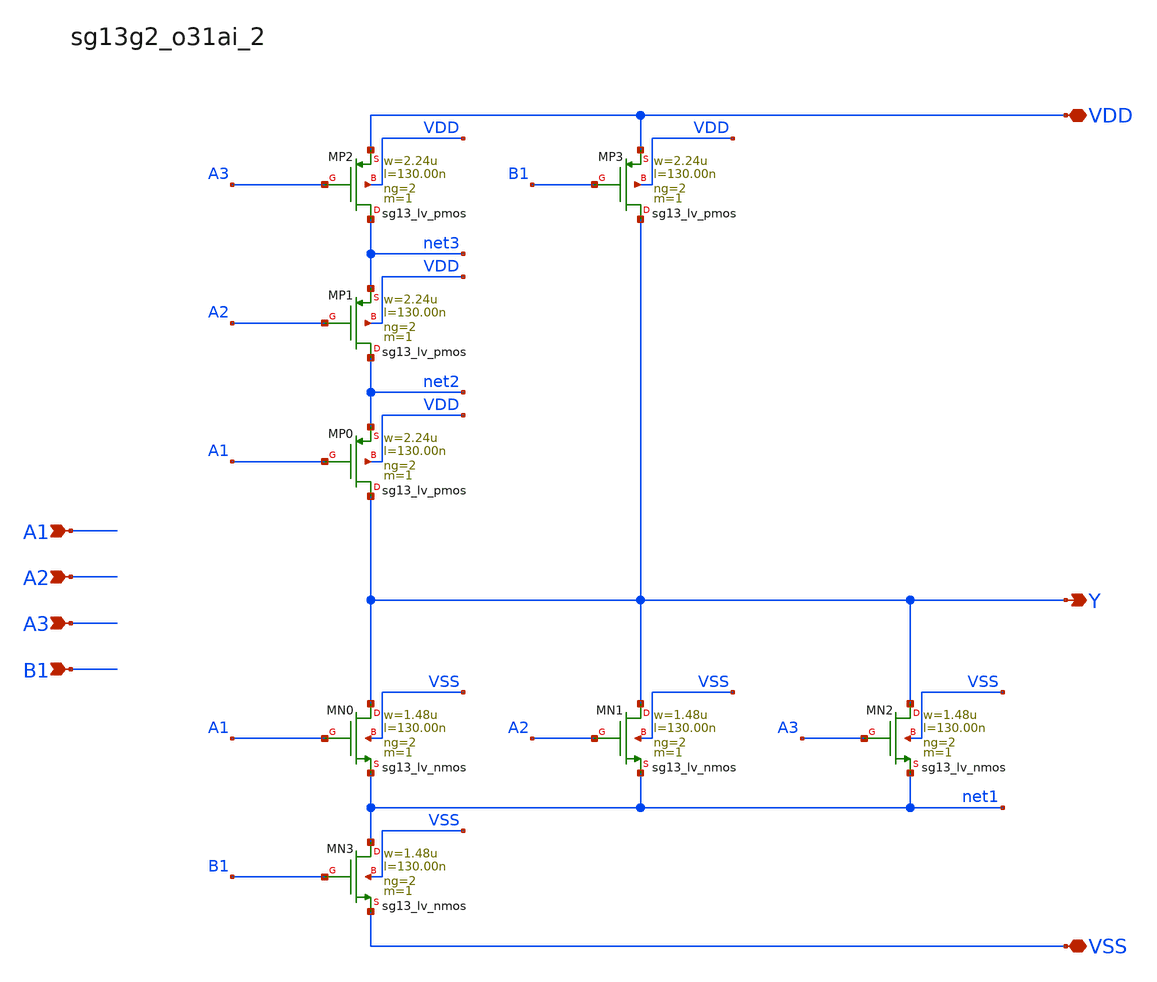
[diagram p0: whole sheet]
** sch_path: outputs/sg13g2_cells/cells/sg13g2_o31ai_2/sg13g2_o31ai_2.sch
**.subckt sg13g2_o31ai_2 Y A1 A2 A3 B1 VDD VSS
*.opin Y
*.ipin A1
*.ipin A2
*.ipin A3
*.ipin B1
*.iopin VDD
*.iopin VSS
XMN0 Y A1 net1 VSS sg13_lv_nmos w=1.48u l=130.00n ng=2 m=1 mm_ok=1
XMN1 Y A2 net1 VSS sg13_lv_nmos w=1.48u l=130.00n ng=2 m=1 mm_ok=1
XMN2 Y A3 net1 VSS sg13_lv_nmos w=1.48u l=130.00n ng=2 m=1 mm_ok=1
XMN3 net1 B1 VSS VSS sg13_lv_nmos w=1.48u l=130.00n ng=2 m=1 mm_ok=1
XMP0 Y A1 net2 VDD sg13_lv_pmos w=2.24u l=130.00n ng=2 m=1 mm_ok=1
XMP1 net2 A2 net3 VDD sg13_lv_pmos w=2.24u l=130.00n ng=2 m=1 mm_ok=1
XMP2 net3 A3 VDD VDD sg13_lv_pmos w=2.24u l=130.00n ng=2 m=1 mm_ok=1
XMP3 Y B1 VDD VDD sg13_lv_pmos w=2.24u l=130.00n ng=2 m=1 mm_ok=1
**.ends
.end
